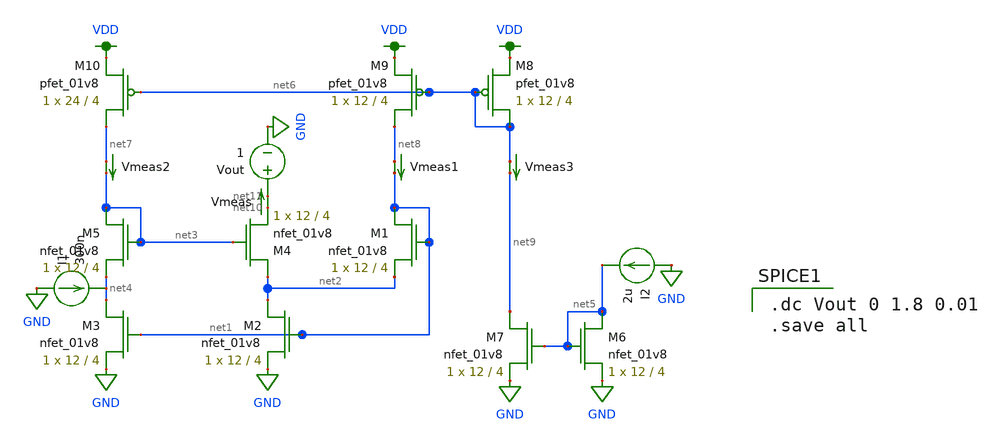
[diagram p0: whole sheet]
** sch_path: testing/test_harness_super_wilson.sch
**.subckt test_harness_super_wilson
I1 GND net4 300n
I2 GND net5 2u
Vmeas net10 net11 0
.save i(vmeas)
Vout net11 GND 1
XM6 net5 net5 GND GND sky130_fd_pr__nfet_01v8 L=4 W=12 nf=1 ad='int((nf+1)/2) * W/nf * 0.29' as='int((nf+2)/2) * W/nf * 0.29'
+ pd='2*int((nf+1)/2) * (W/nf + 0.29)' ps='2*int((nf+2)/2) * (W/nf + 0.29)' nrd='0.29 / W' nrs='0.29 / W'
+ sa=0 sb=0 sd=0 mult=1 m=1
XM9 net8 net6 VDD VDD sky130_fd_pr__pfet_01v8 L=4 W=12 nf=1 ad='int((nf+1)/2) * W/nf * 0.29' as='int((nf+2)/2) * W/nf * 0.29'
+ pd='2*int((nf+1)/2) * (W/nf + 0.29)' ps='2*int((nf+2)/2) * (W/nf + 0.29)' nrd='0.29 / W' nrs='0.29 / W'
+ sa=0 sb=0 sd=0 mult=1 m=1
XM10 net7 net6 VDD VDD sky130_fd_pr__pfet_01v8 L=4 W=24 nf=1 ad='int((nf+1)/2) * W/nf * 0.29' as='int((nf+2)/2) * W/nf * 0.29'
+ pd='2*int((nf+1)/2) * (W/nf + 0.29)' ps='2*int((nf+2)/2) * (W/nf + 0.29)' nrd='0.29 / W' nrs='0.29 / W'
+ sa=0 sb=0 sd=0 mult=1 m=1
XM8 net6 net6 VDD VDD sky130_fd_pr__pfet_01v8 L=4 W=12 nf=1 ad='int((nf+1)/2) * W/nf * 0.29' as='int((nf+2)/2) * W/nf * 0.29'
+ pd='2*int((nf+1)/2) * (W/nf + 0.29)' ps='2*int((nf+2)/2) * (W/nf + 0.29)' nrd='0.29 / W' nrs='0.29 / W'
+ sa=0 sb=0 sd=0 mult=1 m=1
XM7 net9 net5 GND GND sky130_fd_pr__nfet_01v8 L=4 W=12 nf=1 ad='int((nf+1)/2) * W/nf * 0.29' as='int((nf+2)/2) * W/nf * 0.29'
+ pd='2*int((nf+1)/2) * (W/nf + 0.29)' ps='2*int((nf+2)/2) * (W/nf + 0.29)' nrd='0.29 / W' nrs='0.29 / W'
+ sa=0 sb=0 sd=0 mult=1 m=1
XM1 net1 net1 net2 GND sky130_fd_pr__nfet_01v8 L=4 W=12 nf=1 ad='int((nf+1)/2) * W/nf * 0.29' as='int((nf+2)/2) * W/nf * 0.29'
+ pd='2*int((nf+1)/2) * (W/nf + 0.29)' ps='2*int((nf+2)/2) * (W/nf + 0.29)' nrd='0.29 / W' nrs='0.29 / W'
+ sa=0 sb=0 sd=0 mult=1 m=1
XM2 net2 net1 GND GND sky130_fd_pr__nfet_01v8 L=4 W=12 nf=1 ad='int((nf+1)/2) * W/nf * 0.29' as='int((nf+2)/2) * W/nf * 0.29'
+ pd='2*int((nf+1)/2) * (W/nf + 0.29)' ps='2*int((nf+2)/2) * (W/nf + 0.29)' nrd='0.29 / W' nrs='0.29 / W'
+ sa=0 sb=0 sd=0 mult=1 m=1
XM3 net4 net1 GND GND sky130_fd_pr__nfet_01v8 L=4 W=12 nf=1 ad='int((nf+1)/2) * W/nf * 0.29' as='int((nf+2)/2) * W/nf * 0.29'
+ pd='2*int((nf+1)/2) * (W/nf + 0.29)' ps='2*int((nf+2)/2) * (W/nf + 0.29)' nrd='0.29 / W' nrs='0.29 / W'
+ sa=0 sb=0 sd=0 mult=1 m=1
XM5 net3 net3 net4 GND sky130_fd_pr__nfet_01v8 L=4 W=12 nf=1 ad='int((nf+1)/2) * W/nf * 0.29' as='int((nf+2)/2) * W/nf * 0.29'
+ pd='2*int((nf+1)/2) * (W/nf + 0.29)' ps='2*int((nf+2)/2) * (W/nf + 0.29)' nrd='0.29 / W' nrs='0.29 / W'
+ sa=0 sb=0 sd=0 mult=1 m=1
XM4 net2 net3 net10 GND sky130_fd_pr__nfet_01v8 L=4 W=12 nf=1 ad='int((nf+1)/2) * W/nf * 0.29' as='int((nf+2)/2) * W/nf * 0.29'
+ pd='2*int((nf+1)/2) * (W/nf + 0.29)' ps='2*int((nf+2)/2) * (W/nf + 0.29)' nrd='0.29 / W' nrs='0.29 / W'
+ sa=0 sb=0 sd=0 mult=1 m=1
Vmeas1 net8 net1 0
.save i(vmeas1)
Vmeas2 net7 net3 0
.save i(vmeas2)
Vmeas3 net6 net9 0
.save i(vmeas3)
**** begin user architecture code

.option wnflag=1
.param MC_SWITCH=0.0
.lib ~/skywater/skywater-pdk/libraries/sky130_fd_pr_ngspice/latest/models/sky130.lib.spice tt


.dc Vout 0 1.8 0.01
.save all

**** end user architecture code
**.ends
.GLOBAL GND
.GLOBAL VDD
.end
